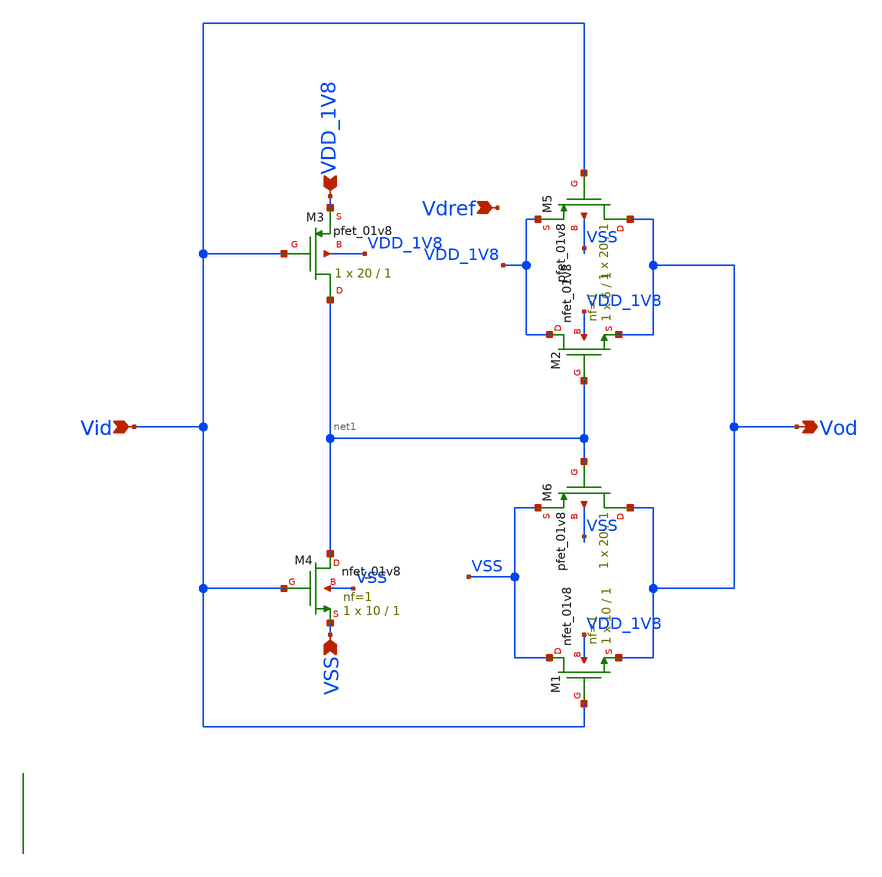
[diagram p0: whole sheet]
** sch_path: design/CNR_GR06_SKY130NM/dac.sch
**.subckt dac VDD_1V8 VSS Vid Vod Vid Vdref
*.ipin VDD_1V8
*.ipin VSS
*.ipin Vid
*.opin Vod
*.ipin Vid
*.ipin Vdref
XM3 net1 Vid VDD_1V8 VDD_1V8 sky130_fd_pr__pfet_01v8 W=20 L=1 ad='int((nf+1)/2) * W/nf * 0.29' pd='2*int((nf+1)/2) * (W/nf + 0.29)'
+ as='int((nf+2)/2) * W/nf * 0.29' ps='2*int((nf+2)/2) * (W/nf + 0.29)' nrd='0.29 / W' nrs='0.29 / W' sa=0
+ sb=0 sd=0 nf=1 mult=1
XM4 net1 Vid VSS VSS sky130_fd_pr__nfet_01v8 L=1 W=10 nf=1 ad='int((nf+1)/2) * W/nf * 0.29' as='int((nf+2)/2) * W/nf * 0.29'
+ pd='2*int((nf+1)/2) * (W/nf + 0.29)' ps='2*int((nf+2)/2) * (W/nf + 0.29)' nrd='0.29 / W' nrs='0.29 / W'
+ sa=0 sb=0 sd=0 mult=1 m=1
XM1 VSS Vid Vod VDD_1V8 sky130_fd_pr__nfet_01v8 L=1 W=10 nf=1 ad='int((nf+1)/2) * W/nf * 0.29' as='int((nf+2)/2) * W/nf * 0.29'
+ pd='2*int((nf+1)/2) * (W/nf + 0.29)' ps='2*int((nf+2)/2) * (W/nf + 0.29)' nrd='0.29 / W' nrs='0.29 / W'
+ sa=0 sb=0 sd=0 mult=1 m=1
XM2 VDD_1V8 net1 Vod VDD_1V8 sky130_fd_pr__nfet_01v8 L=1 W=6 nf=1 ad='int((nf+1)/2) * W/nf * 0.29' as='int((nf+2)/2) * W/nf * 0.29'
+ pd='2*int((nf+1)/2) * (W/nf + 0.29)' ps='2*int((nf+2)/2) * (W/nf + 0.29)' nrd='0.29 / W' nrs='0.29 / W'
+ sa=0 sb=0 sd=0 mult=1 m=1
XM5 Vod Vid VDD_1V8 VSS sky130_fd_pr__pfet_01v8 W=20 L=1 ad='int((nf+1)/2) * W/nf * 0.29' pd='2*int((nf+1)/2) * (W/nf + 0.29)'
+ as='int((nf+2)/2) * W/nf * 0.29' ps='2*int((nf+2)/2) * (W/nf + 0.29)' nrd='0.29 / W' nrs='0.29 / W' sa=0
+ sb=0 sd=0 nf=1 mult=1
XM6 Vod net1 VSS VSS sky130_fd_pr__pfet_01v8 W=20 L=1 ad='int((nf+1)/2) * W/nf * 0.29' pd='2*int((nf+1)/2) * (W/nf + 0.29)'
+ as='int((nf+2)/2) * W/nf * 0.29' ps='2*int((nf+2)/2) * (W/nf + 0.29)' nrd='0.29 / W' nrs='0.29 / W' sa=0
+ sb=0 sd=0 nf=1 mult=1
**.ends
.end
